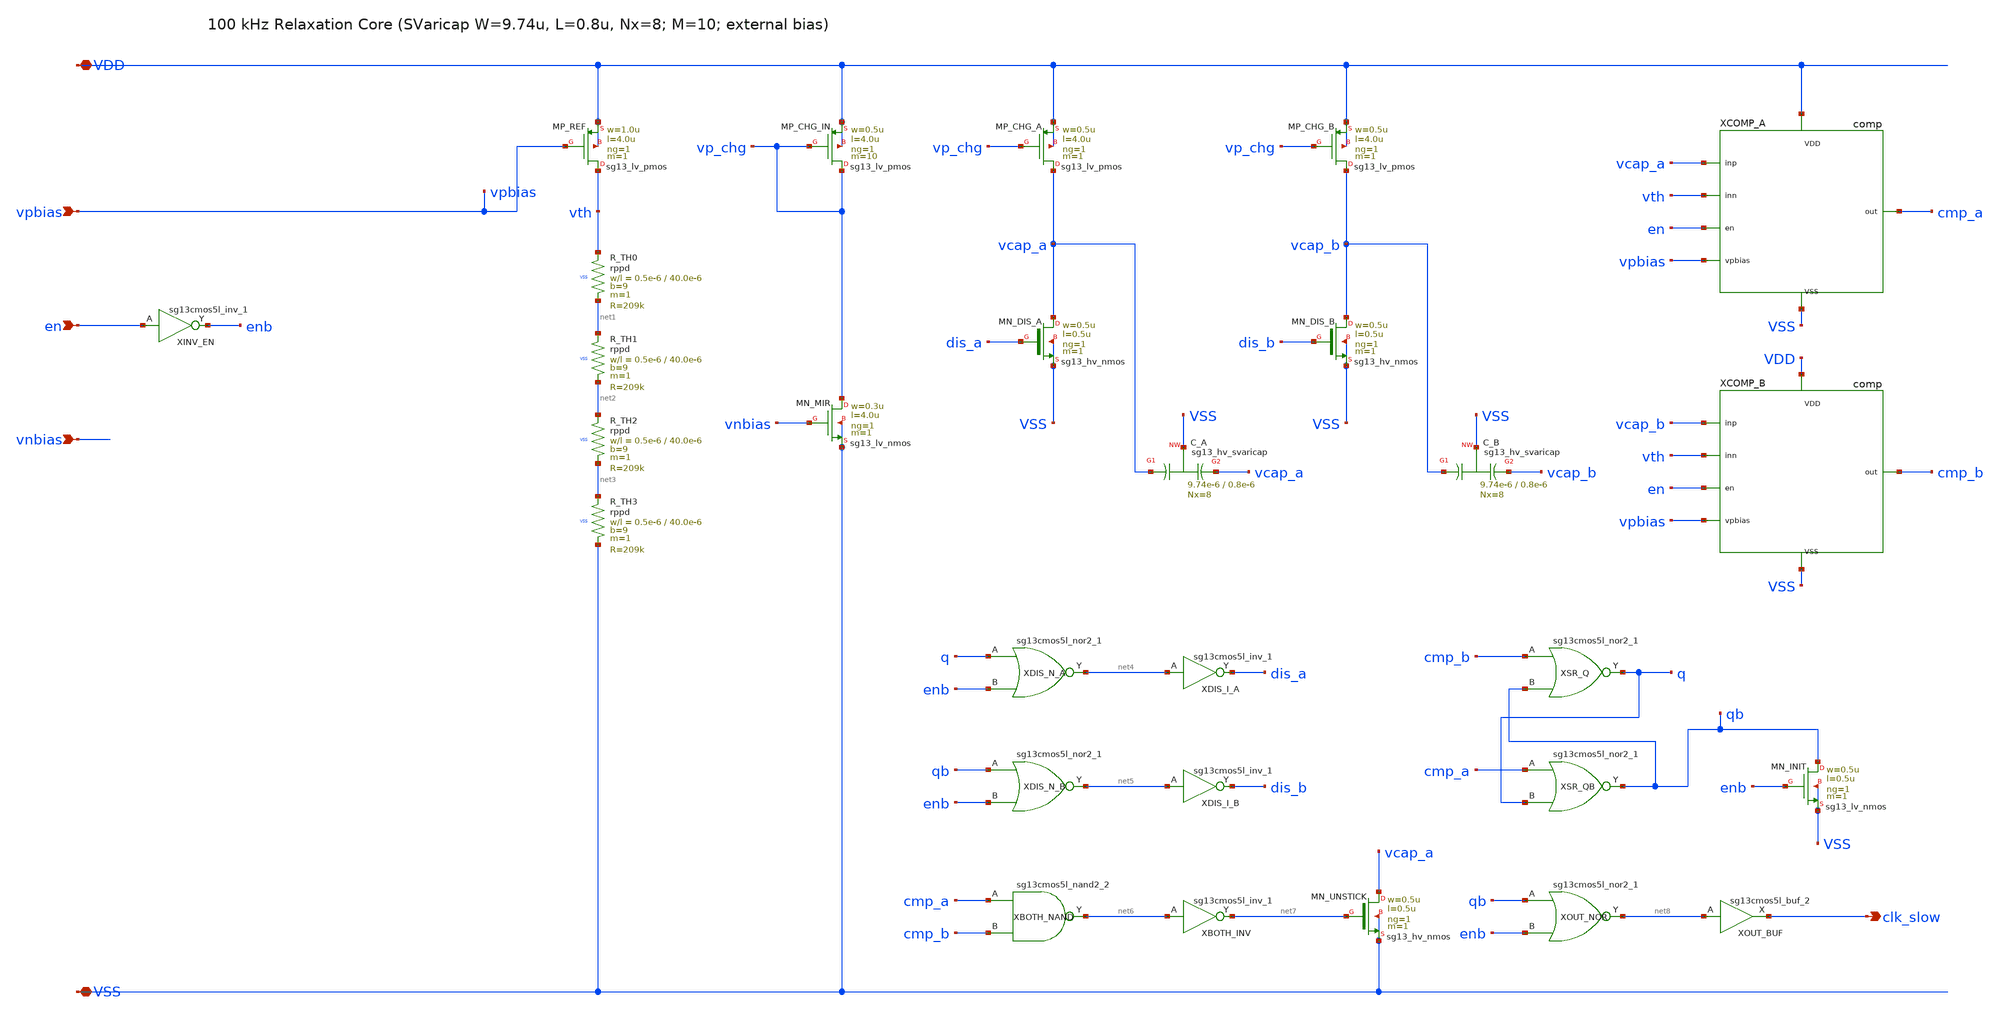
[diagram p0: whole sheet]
** sch_path: analog/clk_macro/relax_core.sch
**.subckt relax_core VDD VSS en vpbias vnbias clk_slow
*.iopin VDD
*.iopin VSS
*.ipin en
*.ipin vpbias
*.ipin vnbias
*.opin clk_slow
XINV_EN enb en VDD VSS sg13cmos5l_inv_1
XMP_REF vth vpbias VDD VDD sg13_lv_pmos w=1.0u l=4.0u ng=1 m=1 mm_ok=1
XR_TH0 vth net1 VSS rppd w=0.5e-6 l=40.0e-6 m=1 b=9 mm_ok=1
XR_TH1 net1 net2 VSS rppd w=0.5e-6 l=40.0e-6 m=1 b=9 mm_ok=1
XR_TH2 net2 net3 VSS rppd w=0.5e-6 l=40.0e-6 m=1 b=9 mm_ok=1
XR_TH3 net3 VSS VSS rppd w=0.5e-6 l=40.0e-6 m=1 b=9 mm_ok=1
XMN_MIR vp_chg vnbias VSS VSS sg13_lv_nmos w=0.3u l=4.0u ng=1 m=1 mm_ok=1
XMP_CHG_IN vp_chg vp_chg VDD VDD sg13_lv_pmos w=0.5u l=4.0u ng=1 m=10 mm_ok=1
XMP_CHG_A vcap_a vp_chg VDD VDD sg13_lv_pmos w=0.5u l=4.0u ng=1 m=1 mm_ok=1
XMN_DIS_A vcap_a dis_a VSS VSS sg13_hv_nmos w=0.5u l=0.5u ng=1 m=1 mm_ok=1
XC_A vcap_a VSS vcap_a VSS sg13_hv_svaricap w=9.74e-6 l=0.8e-6 Nx=8 mm_ok=1
XCOMP_A VDD VSS en vpbias vcap_a vth cmp_a comp
XMP_CHG_B vcap_b vp_chg VDD VDD sg13_lv_pmos w=0.5u l=4.0u ng=1 m=1 mm_ok=1
XMN_DIS_B vcap_b dis_b VSS VSS sg13_hv_nmos w=0.5u l=0.5u ng=1 m=1 mm_ok=1
XC_B vcap_b VSS vcap_b VSS sg13_hv_svaricap w=9.74e-6 l=0.8e-6 Nx=8 mm_ok=1
XCOMP_B VDD VSS en vpbias vcap_b vth cmp_b comp
XSR_Q q cmp_b qb VDD VSS sg13cmos5l_nor2_1
XSR_QB qb cmp_a q VDD VSS sg13cmos5l_nor2_1
XMN_INIT qb enb VSS VSS sg13_lv_nmos w=0.5u l=0.5u ng=1 m=1 mm_ok=1
XDIS_N_A net4 q enb VDD VSS sg13cmos5l_nor2_1
XDIS_I_A dis_a net4 VDD VSS sg13cmos5l_inv_1
XDIS_N_B net5 qb enb VDD VSS sg13cmos5l_nor2_1
XDIS_I_B dis_b net5 VDD VSS sg13cmos5l_inv_1
XBOTH_NAND net6 cmp_a cmp_b VDD VSS sg13cmos5l_nand2_2
XBOTH_INV net7 net6 VDD VSS sg13cmos5l_inv_1
XMN_UNSTICK vcap_a net7 VSS VSS sg13_hv_nmos w=0.5u l=0.5u ng=1 m=1 mm_ok=1
XOUT_NOR net8 qb enb VDD VSS sg13cmos5l_nor2_1
XOUT_BUF clk_slow net8 VDD VSS sg13cmos5l_buf_2
**.ends

* expanding   symbol:  osc_relax/comp.sym # of pins=7
** sym_path: analog/osc_relax/comp.sym
** sch_path: analog/osc_relax/comp.sch
.subckt comp VDD VSS en vpbias inp inn out
*.iopin VDD
*.iopin VSS
*.ipin en
*.ipin vpbias
*.ipin inp
*.ipin inn
*.opin out
XMP_TAIL net1 vpbias VDD VDD sg13_lv_pmos w=1.0u l=4.0u ng=1 m=1 mm_ok=1
XMP_INP net2 inp net1 VDD sg13_lv_pmos w=2.0u l=1.0u ng=1 m=2 mm_ok=1
XMP_INN net3 inn net1 VDD sg13_lv_pmos w=2.0u l=1.0u ng=1 m=2 mm_ok=1
XMN_L1 net2 net2 VSS VSS sg13_lv_nmos w=0.5u l=2.0u ng=1 m=1 mm_ok=1
XMN_L2 net3 net2 VSS VSS sg13_lv_nmos w=0.5u l=2.0u ng=1 m=1 mm_ok=1
XMP_G2 net4 vpbias VDD VDD sg13_lv_pmos w=1.0u l=4.0u ng=1 m=1 mm_ok=1
XMN_G2 net4 net3 VSS VSS sg13_lv_nmos w=1.0u l=1.0u ng=1 m=1 mm_ok=1
XMP_OFF net4 en VDD VDD sg13_lv_pmos w=0.5u l=0.5u ng=1 m=1 mm_ok=1
XINV_OUT out net4 VDD VSS sg13cmos5l_inv_1
.ends

.end
